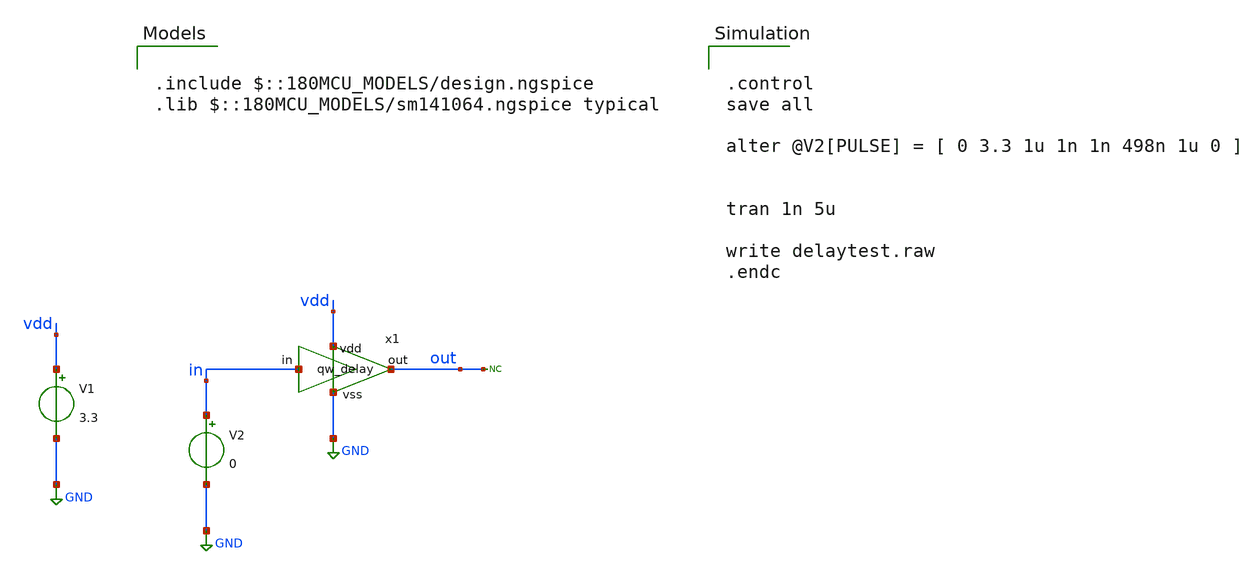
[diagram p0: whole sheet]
** sch_path: designs/libs/qw_core_analog_pkedit/delaytest.sch
**.subckt delaytest
x1 vdd in out GND qw_DELAY
V1 vdd GND 3.3
* noconn out
V2 in GND 0
**** begin user architecture code


.control
save all

alter @V2[PULSE] = [ 0 3.3 1u 1n 1n 498n 1u 0 ]


tran 1n 5u

write delaytest.raw
.endc



.include $::180MCU_MODELS/design.ngspice
.lib $::180MCU_MODELS/sm141064.ngspice typical

**** end user architecture code
**.ends

* expanding   symbol:  qw_DELAY.sym # of pins=4
** sym_path: designs/libs/qw_core_analog_pkedit/qw_DELAY.sym
** sch_path: designs/libs/qw_core_analog_pkedit/qw_DELAY.sch
.subckt qw_DELAY vdd in out vss
*.iopin vdd
*.iopin vss
*.iopin in
*.iopin out
XM1 net1 in vss vss nfet_03v3 L=5u W=1u nf=1 ad='int((nf+1)/2) * W/nf * 0.18u' as='int((nf+2)/2) * W/nf * 0.18u'
+ pd='2*int((nf+1)/2) * (W/nf + 0.18u)' ps='2*int((nf+2)/2) * (W/nf + 0.18u)' nrd='0.18u / W' nrs='0.18u / W'
+ sa=0 sb=0 sd=0 m=1
XM2 net1 in vdd vdd pfet_03v3 L=5u W=2u nf=1 ad='int((nf+1)/2) * W/nf * 0.18u' as='int((nf+2)/2) * W/nf * 0.18u'
+ pd='2*int((nf+1)/2) * (W/nf + 0.18u)' ps='2*int((nf+2)/2) * (W/nf + 0.18u)' nrd='0.18u / W' nrs='0.18u / W'
+ sa=0 sb=0 sd=0 m=1
XM3 net2 net1 vss vss nfet_03v3 L=5u W=1u nf=1 ad='int((nf+1)/2) * W/nf * 0.18u' as='int((nf+2)/2) * W/nf * 0.18u'
+ pd='2*int((nf+1)/2) * (W/nf + 0.18u)' ps='2*int((nf+2)/2) * (W/nf + 0.18u)' nrd='0.18u / W' nrs='0.18u / W'
+ sa=0 sb=0 sd=0 m=1
XM4 net2 net1 vdd vdd pfet_03v3 L=5u W=2u nf=1 ad='int((nf+1)/2) * W/nf * 0.18u' as='int((nf+2)/2) * W/nf * 0.18u'
+ pd='2*int((nf+1)/2) * (W/nf + 0.18u)' ps='2*int((nf+2)/2) * (W/nf + 0.18u)' nrd='0.18u / W' nrs='0.18u / W'
+ sa=0 sb=0 sd=0 m=1
XM5 net3 net2 vss vss nfet_03v3 L=5u W=1u nf=1 ad='int((nf+1)/2) * W/nf * 0.18u' as='int((nf+2)/2) * W/nf * 0.18u'
+ pd='2*int((nf+1)/2) * (W/nf + 0.18u)' ps='2*int((nf+2)/2) * (W/nf + 0.18u)' nrd='0.18u / W' nrs='0.18u / W'
+ sa=0 sb=0 sd=0 m=1
XM6 net3 net2 vdd vdd pfet_03v3 L=5u W=2u nf=1 ad='int((nf+1)/2) * W/nf * 0.18u' as='int((nf+2)/2) * W/nf * 0.18u'
+ pd='2*int((nf+1)/2) * (W/nf + 0.18u)' ps='2*int((nf+2)/2) * (W/nf + 0.18u)' nrd='0.18u / W' nrs='0.18u / W'
+ sa=0 sb=0 sd=0 m=1
XM7 net4 net3 vss vss nfet_03v3 L=5u W=1u nf=1 ad='int((nf+1)/2) * W/nf * 0.18u' as='int((nf+2)/2) * W/nf * 0.18u'
+ pd='2*int((nf+1)/2) * (W/nf + 0.18u)' ps='2*int((nf+2)/2) * (W/nf + 0.18u)' nrd='0.18u / W' nrs='0.18u / W'
+ sa=0 sb=0 sd=0 m=1
XM8 net4 net3 vdd vdd pfet_03v3 L=5u W=2u nf=1 ad='int((nf+1)/2) * W/nf * 0.18u' as='int((nf+2)/2) * W/nf * 0.18u'
+ pd='2*int((nf+1)/2) * (W/nf + 0.18u)' ps='2*int((nf+2)/2) * (W/nf + 0.18u)' nrd='0.18u / W' nrs='0.18u / W'
+ sa=0 sb=0 sd=0 m=1
XM9 net5 net4 vss vss nfet_03v3 L=5u W=1u nf=1 ad='int((nf+1)/2) * W/nf * 0.18u' as='int((nf+2)/2) * W/nf * 0.18u'
+ pd='2*int((nf+1)/2) * (W/nf + 0.18u)' ps='2*int((nf+2)/2) * (W/nf + 0.18u)' nrd='0.18u / W' nrs='0.18u / W'
+ sa=0 sb=0 sd=0 m=1
XM10 net5 net4 vdd vdd pfet_03v3 L=5u W=2u nf=1 ad='int((nf+1)/2) * W/nf * 0.18u' as='int((nf+2)/2) * W/nf * 0.18u'
+ pd='2*int((nf+1)/2) * (W/nf + 0.18u)' ps='2*int((nf+2)/2) * (W/nf + 0.18u)' nrd='0.18u / W' nrs='0.18u / W'
+ sa=0 sb=0 sd=0 m=1
XM11 out net5 vss vss nfet_03v3 L=5u W=1u nf=1 ad='int((nf+1)/2) * W/nf * 0.18u' as='int((nf+2)/2) * W/nf * 0.18u'
+ pd='2*int((nf+1)/2) * (W/nf + 0.18u)' ps='2*int((nf+2)/2) * (W/nf + 0.18u)' nrd='0.18u / W' nrs='0.18u / W'
+ sa=0 sb=0 sd=0 m=1
XM12 out net5 vdd vdd pfet_03v3 L=5u W=2u nf=1 ad='int((nf+1)/2) * W/nf * 0.18u' as='int((nf+2)/2) * W/nf * 0.18u'
+ pd='2*int((nf+1)/2) * (W/nf + 0.18u)' ps='2*int((nf+2)/2) * (W/nf + 0.18u)' nrd='0.18u / W' nrs='0.18u / W'
+ sa=0 sb=0 sd=0 m=1
.ends

.GLOBAL GND
.end
